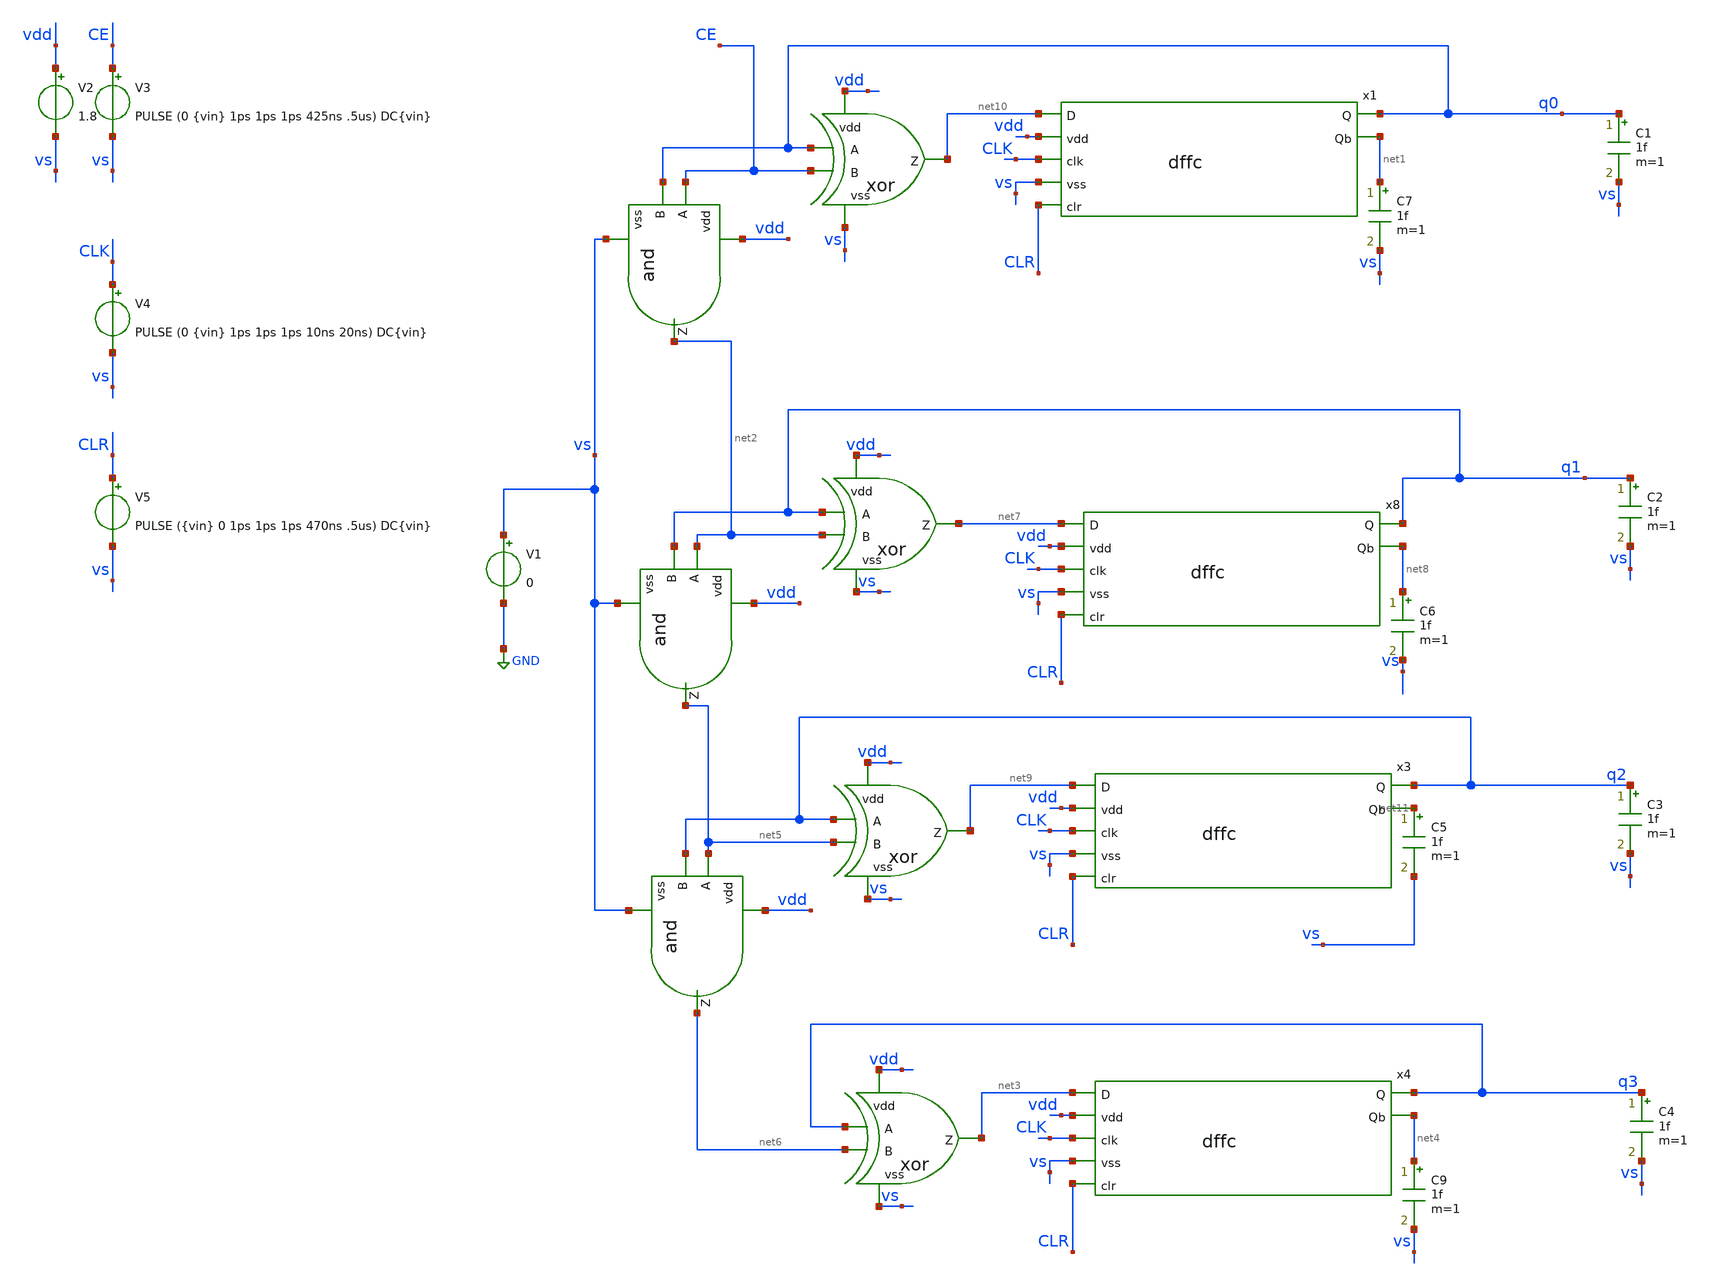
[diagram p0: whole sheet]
** sch_path: track_vlsi/lado/sch/tb_counter_lado.sch
**.subckt tb_counter_lado
x1 net10 q0 vdd CLK vs net1 CLR dffc
xor vdd q0 CE net10 vs xor
x2 vdd CE q0 net2 vs and
V2 vdd vs 1.8
V3 CE vs PULSE (0 {vin} 1ps 1ps 1ps 425ns .5us) DC{vin}
V4 CLK vs PULSE (0 {vin} 1ps 1ps 1ps 10ns 20ns) DC{vin}
V5 CLR vs PULSE ({vin} 0 1ps 1ps 1ps 470ns .5us) DC{vin}
xor4 vdd q1 net2 net7 vs xor
x5 vdd net2 q1 net5 vs and
xor5 vdd q2 net5 net9 vs xor
x6 vdd net5 q2 net6 vs and
xor8 vdd q3 net6 net3 vs xor
C1 q0 vs 1f m=1
C2 q1 vs 1f m=1
C3 q2 vs 1f m=1
C4 q3 vs 1f m=1
x8 net7 q1 vdd CLK vs net8 CLR dffc
x3 net9 q2 vdd CLK vs net11 CLR dffc
x4 net3 q3 vdd CLK vs net4 CLR dffc
V1 vs GND 0
C5 net11 vs 1f m=1
C6 net8 vs 1f m=1
C7 net1 vs 1f m=1
C9 net4 vs 1f m=1
**** begin user architecture code



*parametros
.param vin=1.8
.options TEMP=27.0

*include

.lib /home/eamta/skywater/skywater-pdk/libraries/sky130_fd_pr_ngspice/latest/models/corners/sky130.lib TT

*signals to save
.save all
*+ @m.x1.xm2.msky130_fd_pr__nfet_01v8[id] @m.x1.xm2.msky130_fd_pr__nfet_01v8[gm]
*+ @m.x1.xm1.msky130_fd_pr__pfet_01v8[id] @m.x1.xm1.msky130_fd_pr__pfet_01v8[gm]




*config simulacion

.control
  tran 0.1ns 0.5us
  setplot tran1
  plot v(q3) v(q2)+2 v(q1)+4 v(q0)+6 v(CLR)+8 v(CE)+10 v(CLK)+12
  write tb_inverter_trans.raw
  gnuplot salida v(CLK) v(q0)+2 v(q1)+4 v(q2)+6 v(q3)+8 v(CE)+10 v(CLR)+12
  reset
  dc V3 0 1.8 0.01
  setplot dc1
  plot v(q1) v(CLk)
  write tb_inverter_dc.raw
  reset
  op
  print all

.endc

.end


**** end user architecture code
**.ends

* expanding   symbol:  dffc.sym # of pins=7
** sym_path: track_vlsi/lado/sch/dffc.sym
** sch_path: track_vlsi/lado/sch/dffc.sch
.subckt dffc D Q vdd clk vss Qb clr
*.ipin clk
*.ipin vdd
*.ipin vss
*.ipin D
*.opin Q
*.opin Qb
*.ipin clr
XM0 net1 nclk D vdd sky130_fd_pr__pfet_01v8 L=0.15 W=1.5 nf=1 ad='int((nf+1)/2) * W/nf * 0.29' as='int((nf+2)/2) * W/nf * 0.29'
+ pd='2*int((nf+1)/2) * (W/nf + 0.29)' ps='2*int((nf+2)/2) * (W/nf + 0.29)' nrd='0.29 / W' nrs='0.29 / W'
+ sa=0 sb=0 sd=0 mult=1 m=1
XM1 net1 clk D vss sky130_fd_pr__nfet_01v8 L=0.15 W=1.5 nf=1 ad='int((nf+1)/2) * W/nf * 0.29' as='int((nf+2)/2) * W/nf * 0.29'
+ pd='2*int((nf+1)/2) * (W/nf + 0.29)' ps='2*int((nf+2)/2) * (W/nf + 0.29)' nrd='0.29 / W' nrs='0.29 / W'
+ sa=0 sb=0 sd=0 mult=1 m=1
XM2 net2 net4 vdd vdd sky130_fd_pr__pfet_01v8 L=0.15 W=1.5 nf=1 ad='int((nf+1)/2) * W/nf * 0.29' as='int((nf+2)/2) * W/nf * 0.29'
+ pd='2*int((nf+1)/2) * (W/nf + 0.29)' ps='2*int((nf+2)/2) * (W/nf + 0.29)' nrd='0.29 / W' nrs='0.29 / W'
+ sa=0 sb=0 sd=0 mult=1 m=1
XM5 net3 clr vss vss sky130_fd_pr__nfet_01v8 L=0.15 W=1.5 nf=1 ad='int((nf+1)/2) * W/nf * 0.29' as='int((nf+2)/2) * W/nf * 0.29'
+ pd='2*int((nf+1)/2) * (W/nf + 0.29)' ps='2*int((nf+2)/2) * (W/nf + 0.29)' nrd='0.29 / W' nrs='0.29 / W'
+ sa=0 sb=0 sd=0 mult=1 m=1
XM6 net3 clr net2 vdd sky130_fd_pr__pfet_01v8 L=0.15 W=1.5 nf=1 ad='int((nf+1)/2) * W/nf * 0.29' as='int((nf+2)/2) * W/nf * 0.29'
+ pd='2*int((nf+1)/2) * (W/nf + 0.29)' ps='2*int((nf+2)/2) * (W/nf + 0.29)' nrd='0.29 / W' nrs='0.29 / W'
+ sa=0 sb=0 sd=0 mult=1 m=1
XM14 net5 clk net4 vdd sky130_fd_pr__pfet_01v8 L=0.15 W=1.5 nf=1 ad='int((nf+1)/2) * W/nf * 0.29' as='int((nf+2)/2) * W/nf * 0.29'
+ pd='2*int((nf+1)/2) * (W/nf + 0.29)' ps='2*int((nf+2)/2) * (W/nf + 0.29)' nrd='0.29 / W' nrs='0.29 / W'
+ sa=0 sb=0 sd=0 mult=1 m=1
XM15 net5 nclk net4 vss sky130_fd_pr__nfet_01v8 L=0.15 W=1.5 nf=1 ad='int((nf+1)/2) * W/nf * 0.29' as='int((nf+2)/2) * W/nf * 0.29'
+ pd='2*int((nf+1)/2) * (W/nf + 0.29)' ps='2*int((nf+2)/2) * (W/nf + 0.29)' nrd='0.29 / W' nrs='0.29 / W'
+ sa=0 sb=0 sd=0 mult=1 m=1
XM7 net3 net4 vss vss sky130_fd_pr__nfet_01v8 L=0.15 W=1.5 nf=1 ad='int((nf+1)/2) * W/nf * 0.29' as='int((nf+2)/2) * W/nf * 0.29'
+ pd='2*int((nf+1)/2) * (W/nf + 0.29)' ps='2*int((nf+2)/2) * (W/nf + 0.29)' nrd='0.29 / W' nrs='0.29 / W'
+ sa=0 sb=0 sd=0 mult=1 m=1
XM3 net3 clk net1 vdd sky130_fd_pr__pfet_01v8 L=0.15 W=1.5 nf=1 ad='int((nf+1)/2) * W/nf * 0.29' as='int((nf+2)/2) * W/nf * 0.29'
+ pd='2*int((nf+1)/2) * (W/nf + 0.29)' ps='2*int((nf+2)/2) * (W/nf + 0.29)' nrd='0.29 / W' nrs='0.29 / W'
+ sa=0 sb=0 sd=0 mult=1 m=1
XM4 net3 nclk net1 vss sky130_fd_pr__nfet_01v8 L=0.15 W=1.5 nf=1 ad='int((nf+1)/2) * W/nf * 0.29' as='int((nf+2)/2) * W/nf * 0.29'
+ pd='2*int((nf+1)/2) * (W/nf + 0.29)' ps='2*int((nf+2)/2) * (W/nf + 0.29)' nrd='0.29 / W' nrs='0.29 / W'
+ sa=0 sb=0 sd=0 mult=1 m=1
XM8 net6 clr vdd vdd sky130_fd_pr__pfet_01v8 L=0.15 W=1.5 nf=1 ad='int((nf+1)/2) * W/nf * 0.29' as='int((nf+2)/2) * W/nf * 0.29'
+ pd='2*int((nf+1)/2) * (W/nf + 0.29)' ps='2*int((nf+2)/2) * (W/nf + 0.29)' nrd='0.29 / W' nrs='0.29 / W'
+ sa=0 sb=0 sd=0 mult=1 m=1
XM9 Q net5 vss vss sky130_fd_pr__nfet_01v8 L=0.15 W=1.5 nf=1 ad='int((nf+1)/2) * W/nf * 0.29' as='int((nf+2)/2) * W/nf * 0.29'
+ pd='2*int((nf+1)/2) * (W/nf + 0.29)' ps='2*int((nf+2)/2) * (W/nf + 0.29)' nrd='0.29 / W' nrs='0.29 / W'
+ sa=0 sb=0 sd=0 mult=1 m=1
XM10 Q net5 net6 vdd sky130_fd_pr__pfet_01v8 L=0.15 W=1.5 nf=1 ad='int((nf+1)/2) * W/nf * 0.29' as='int((nf+2)/2) * W/nf * 0.29'
+ pd='2*int((nf+1)/2) * (W/nf + 0.29)' ps='2*int((nf+2)/2) * (W/nf + 0.29)' nrd='0.29 / W' nrs='0.29 / W'
+ sa=0 sb=0 sd=0 mult=1 m=1
XM11 Q clr vss vss sky130_fd_pr__nfet_01v8 L=0.15 W=1.5 nf=1 ad='int((nf+1)/2) * W/nf * 0.29' as='int((nf+2)/2) * W/nf * 0.29'
+ pd='2*int((nf+1)/2) * (W/nf + 0.29)' ps='2*int((nf+2)/2) * (W/nf + 0.29)' nrd='0.29 / W' nrs='0.29 / W'
+ sa=0 sb=0 sd=0 mult=1 m=1
XM12 Qb nclk net5 vdd sky130_fd_pr__pfet_01v8 L=0.15 W=1.5 nf=1 ad='int((nf+1)/2) * W/nf * 0.29' as='int((nf+2)/2) * W/nf * 0.29'
+ pd='2*int((nf+1)/2) * (W/nf + 0.29)' ps='2*int((nf+2)/2) * (W/nf + 0.29)' nrd='0.29 / W' nrs='0.29 / W'
+ sa=0 sb=0 sd=0 mult=1 m=1
XM13 Qb clk net5 vss sky130_fd_pr__nfet_01v8 L=0.15 W=1.5 nf=1 ad='int((nf+1)/2) * W/nf * 0.29' as='int((nf+2)/2) * W/nf * 0.29'
+ pd='2*int((nf+1)/2) * (W/nf + 0.29)' ps='2*int((nf+2)/2) * (W/nf + 0.29)' nrd='0.29 / W' nrs='0.29 / W'
+ sa=0 sb=0 sd=0 mult=1 m=1
XM16 nclk clk vdd vdd sky130_fd_pr__pfet_01v8 L=0.15 W=1.5 nf=1 ad='int((nf+1)/2) * W/nf * 0.29' as='int((nf+2)/2) * W/nf * 0.29'
+ pd='2*int((nf+1)/2) * (W/nf + 0.29)' ps='2*int((nf+2)/2) * (W/nf + 0.29)' nrd='0.29 / W' nrs='0.29 / W'
+ sa=0 sb=0 sd=0 mult=1 m=1
XM17 nclk clk vss vss sky130_fd_pr__nfet_01v8 L=0.15 W=1.5 nf=1 ad='int((nf+1)/2) * W/nf * 0.29' as='int((nf+2)/2) * W/nf * 0.29'
+ pd='2*int((nf+1)/2) * (W/nf + 0.29)' ps='2*int((nf+2)/2) * (W/nf + 0.29)' nrd='0.29 / W' nrs='0.29 / W'
+ sa=0 sb=0 sd=0 mult=1 m=1
XM18 net4 net1 vdd vdd sky130_fd_pr__pfet_01v8 L=0.15 W=1.5 nf=1 ad='int((nf+1)/2) * W/nf * 0.29' as='int((nf+2)/2) * W/nf * 0.29'
+ pd='2*int((nf+1)/2) * (W/nf + 0.29)' ps='2*int((nf+2)/2) * (W/nf + 0.29)' nrd='0.29 / W' nrs='0.29 / W'
+ sa=0 sb=0 sd=0 mult=1 m=1
XM19 net4 net1 vss vss sky130_fd_pr__nfet_01v8 L=0.15 W=1.5 nf=1 ad='int((nf+1)/2) * W/nf * 0.29' as='int((nf+2)/2) * W/nf * 0.29'
+ pd='2*int((nf+1)/2) * (W/nf + 0.29)' ps='2*int((nf+2)/2) * (W/nf + 0.29)' nrd='0.29 / W' nrs='0.29 / W'
+ sa=0 sb=0 sd=0 mult=1 m=1
XM20 Qb Q vdd vdd sky130_fd_pr__pfet_01v8 L=0.15 W=1.5 nf=1 ad='int((nf+1)/2) * W/nf * 0.29' as='int((nf+2)/2) * W/nf * 0.29'
+ pd='2*int((nf+1)/2) * (W/nf + 0.29)' ps='2*int((nf+2)/2) * (W/nf + 0.29)' nrd='0.29 / W' nrs='0.29 / W'
+ sa=0 sb=0 sd=0 mult=1 m=1
XM21 Qb Q vss vss sky130_fd_pr__nfet_01v8 L=0.15 W=1.5 nf=1 ad='int((nf+1)/2) * W/nf * 0.29' as='int((nf+2)/2) * W/nf * 0.29'
+ pd='2*int((nf+1)/2) * (W/nf + 0.29)' ps='2*int((nf+2)/2) * (W/nf + 0.29)' nrd='0.29 / W' nrs='0.29 / W'
+ sa=0 sb=0 sd=0 mult=1 m=1
.ends


* expanding   symbol:  xor.sym # of pins=5
** sym_path: track_vlsi/lado/sch/xor.sym
** sch_path: track_vlsi/lado/sch/xor.sch
.subckt xor vdd A B Z vss
*.ipin A
*.ipin vss
*.ipin vdd
*.opin Z
*.ipin B
XM0 net1 Bb vdd vdd sky130_fd_pr__pfet_01v8 L=0.15 W=0.9 nf=1 ad='int((nf+1)/2) * W/nf * 0.29' as='int((nf+2)/2) * W/nf * 0.29'
+ pd='2*int((nf+1)/2) * (W/nf + 0.29)' ps='2*int((nf+2)/2) * (W/nf + 0.29)' nrd='0.29 / W' nrs='0.29 / W'
+ sa=0 sb=0 sd=0 mult=1 m=1
XM5 Z A net3 vss sky130_fd_pr__nfet_01v8 L=0.15 W=0.9 nf=1 ad='int((nf+1)/2) * W/nf * 0.29' as='int((nf+2)/2) * W/nf * 0.29'
+ pd='2*int((nf+1)/2) * (W/nf + 0.29)' ps='2*int((nf+2)/2) * (W/nf + 0.29)' nrd='0.29 / W' nrs='0.29 / W'
+ sa=0 sb=0 sd=0 mult=1 m=1
XM1 net1 Ab vdd vdd sky130_fd_pr__pfet_01v8 L=0.15 W=0.9 nf=1 ad='int((nf+1)/2) * W/nf * 0.29' as='int((nf+2)/2) * W/nf * 0.29'
+ pd='2*int((nf+1)/2) * (W/nf + 0.29)' ps='2*int((nf+2)/2) * (W/nf + 0.29)' nrd='0.29 / W' nrs='0.29 / W'
+ sa=0 sb=0 sd=0 mult=1 m=1
XM2 Z A net1 vdd sky130_fd_pr__pfet_01v8 L=0.15 W=0.9 nf=1 ad='int((nf+1)/2) * W/nf * 0.29' as='int((nf+2)/2) * W/nf * 0.29'
+ pd='2*int((nf+1)/2) * (W/nf + 0.29)' ps='2*int((nf+2)/2) * (W/nf + 0.29)' nrd='0.29 / W' nrs='0.29 / W'
+ sa=0 sb=0 sd=0 mult=1 m=1
XM4 Z Ab net2 vss sky130_fd_pr__nfet_01v8 L=0.15 W=0.9 nf=1 ad='int((nf+1)/2) * W/nf * 0.29' as='int((nf+2)/2) * W/nf * 0.29'
+ pd='2*int((nf+1)/2) * (W/nf + 0.29)' ps='2*int((nf+2)/2) * (W/nf + 0.29)' nrd='0.29 / W' nrs='0.29 / W'
+ sa=0 sb=0 sd=0 mult=1 m=1
XM6 net2 Bb vss vss sky130_fd_pr__nfet_01v8 L=0.15 W=0.9 nf=1 ad='int((nf+1)/2) * W/nf * 0.29' as='int((nf+2)/2) * W/nf * 0.29'
+ pd='2*int((nf+1)/2) * (W/nf + 0.29)' ps='2*int((nf+2)/2) * (W/nf + 0.29)' nrd='0.29 / W' nrs='0.29 / W'
+ sa=0 sb=0 sd=0 mult=1 m=1
XM8 Ab A vdd vdd sky130_fd_pr__pfet_01v8 L=0.15 W=0.9 nf=1 ad='int((nf+1)/2) * W/nf * 0.29' as='int((nf+2)/2) * W/nf * 0.29'
+ pd='2*int((nf+1)/2) * (W/nf + 0.29)' ps='2*int((nf+2)/2) * (W/nf + 0.29)' nrd='0.29 / W' nrs='0.29 / W'
+ sa=0 sb=0 sd=0 mult=1 m=1
XM9 Ab A vss vss sky130_fd_pr__nfet_01v8 L=0.15 W=0.45 nf=1 ad='int((nf+1)/2) * W/nf * 0.29' as='int((nf+2)/2) * W/nf * 0.29'
+ pd='2*int((nf+1)/2) * (W/nf + 0.29)' ps='2*int((nf+2)/2) * (W/nf + 0.29)' nrd='0.29 / W' nrs='0.29 / W'
+ sa=0 sb=0 sd=0 mult=1 m=1
XM3 Z B net1 vdd sky130_fd_pr__pfet_01v8 L=0.15 W=0.9 nf=1 ad='int((nf+1)/2) * W/nf * 0.29' as='int((nf+2)/2) * W/nf * 0.29'
+ pd='2*int((nf+1)/2) * (W/nf + 0.29)' ps='2*int((nf+2)/2) * (W/nf + 0.29)' nrd='0.29 / W' nrs='0.29 / W'
+ sa=0 sb=0 sd=0 mult=1 m=1
XM12 Bb B vss vss sky130_fd_pr__nfet_01v8 L=0.15 W=0.45 nf=1 ad='int((nf+1)/2) * W/nf * 0.29' as='int((nf+2)/2) * W/nf * 0.29'
+ pd='2*int((nf+1)/2) * (W/nf + 0.29)' ps='2*int((nf+2)/2) * (W/nf + 0.29)' nrd='0.29 / W' nrs='0.29 / W'
+ sa=0 sb=0 sd=0 mult=1 m=1
XM7 net3 B vss vss sky130_fd_pr__nfet_01v8 L=0.15 W=0.9 nf=1 ad='int((nf+1)/2) * W/nf * 0.29' as='int((nf+2)/2) * W/nf * 0.29'
+ pd='2*int((nf+1)/2) * (W/nf + 0.29)' ps='2*int((nf+2)/2) * (W/nf + 0.29)' nrd='0.29 / W' nrs='0.29 / W'
+ sa=0 sb=0 sd=0 mult=1 m=1
XM10 Bb B vdd vdd sky130_fd_pr__pfet_01v8 L=0.15 W=0.9 nf=1 ad='int((nf+1)/2) * W/nf * 0.29' as='int((nf+2)/2) * W/nf * 0.29'
+ pd='2*int((nf+1)/2) * (W/nf + 0.29)' ps='2*int((nf+2)/2) * (W/nf + 0.29)' nrd='0.29 / W' nrs='0.29 / W'
+ sa=0 sb=0 sd=0 mult=1 m=1
.ends


* expanding   symbol:  and.sym # of pins=5
** sym_path: track_vlsi/lado/sch/and.sym
** sch_path: track_vlsi/lado/sch/and.sch
.subckt and vdd A B Z vss
*.opin Z
*.ipin vdd
*.ipin A
*.ipin vss
*.ipin B
XM1 Z net1 vdd vdd sky130_fd_pr__pfet_01v8 L=0.15 W=0.9 nf=1 ad='int((nf+1)/2) * W/nf * 0.29' as='int((nf+2)/2) * W/nf * 0.29'
+ pd='2*int((nf+1)/2) * (W/nf + 0.29)' ps='2*int((nf+2)/2) * (W/nf + 0.29)' nrd='0.29 / W' nrs='0.29 / W'
+ sa=0 sb=0 sd=0 mult=1 m=1
XM2 Z net1 vss vss sky130_fd_pr__nfet_01v8 L=0.15 W=0.45 nf=1 ad='int((nf+1)/2) * W/nf * 0.29' as='int((nf+2)/2) * W/nf * 0.29'
+ pd='2*int((nf+1)/2) * (W/nf + 0.29)' ps='2*int((nf+2)/2) * (W/nf + 0.29)' nrd='0.29 / W' nrs='0.29 / W'
+ sa=0 sb=0 sd=0 mult=1 m=1
XM3 net1 A vdd vdd sky130_fd_pr__pfet_01v8 L=0.15 W=0.9 nf=1 ad='int((nf+1)/2) * W/nf * 0.29' as='int((nf+2)/2) * W/nf * 0.29'
+ pd='2*int((nf+1)/2) * (W/nf + 0.29)' ps='2*int((nf+2)/2) * (W/nf + 0.29)' nrd='0.29 / W' nrs='0.29 / W'
+ sa=0 sb=0 sd=0 mult=1 m=1
XM4 net1 B vdd vdd sky130_fd_pr__pfet_01v8 L=0.15 W=0.9 nf=1 ad='int((nf+1)/2) * W/nf * 0.29' as='int((nf+2)/2) * W/nf * 0.29'
+ pd='2*int((nf+1)/2) * (W/nf + 0.29)' ps='2*int((nf+2)/2) * (W/nf + 0.29)' nrd='0.29 / W' nrs='0.29 / W'
+ sa=0 sb=0 sd=0 mult=1 m=1
XM5 net1 A net2 vss sky130_fd_pr__nfet_01v8 L=0.15 W=0.9 nf=1 ad='int((nf+1)/2) * W/nf * 0.29' as='int((nf+2)/2) * W/nf * 0.29'
+ pd='2*int((nf+1)/2) * (W/nf + 0.29)' ps='2*int((nf+2)/2) * (W/nf + 0.29)' nrd='0.29 / W' nrs='0.29 / W'
+ sa=0 sb=0 sd=0 mult=1 m=1
XM6 net2 B vss vss sky130_fd_pr__nfet_01v8 L=0.15 W=0.9 nf=1 ad='int((nf+1)/2) * W/nf * 0.29' as='int((nf+2)/2) * W/nf * 0.29'
+ pd='2*int((nf+1)/2) * (W/nf + 0.29)' ps='2*int((nf+2)/2) * (W/nf + 0.29)' nrd='0.29 / W' nrs='0.29 / W'
+ sa=0 sb=0 sd=0 mult=1 m=1
.ends

.GLOBAL GND
.end
